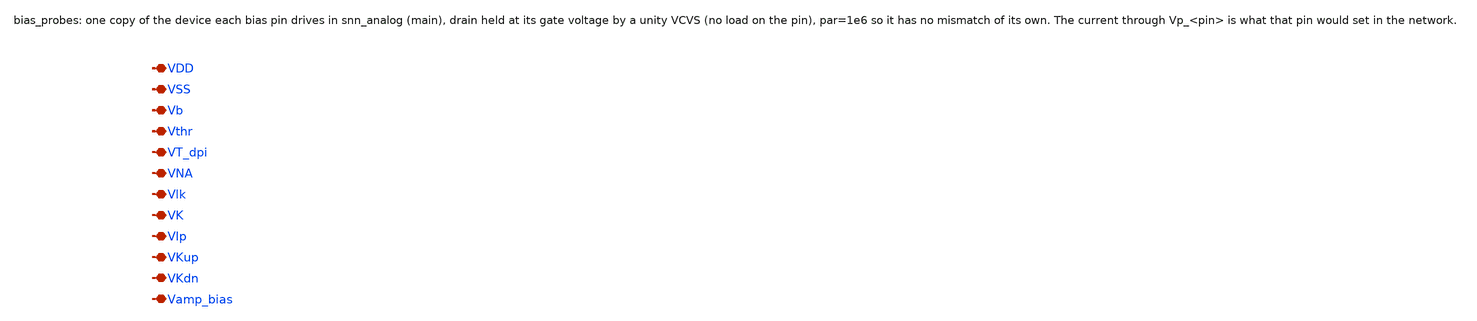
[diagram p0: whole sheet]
** sch_path: analog/bias/testbenches/bias_probes.sch
**.subckt bias_probes VDD VSS Vb Vthr VT_dpi VNA Vlk VK VIp VKup VKdn Vamp_bias
*.iopin VDD
*.iopin VSS
*.iopin Vb
*.iopin Vthr
*.iopin VT_dpi
*.iopin VNA
*.iopin Vlk
*.iopin VK
*.iopin VIp
*.iopin VKup
*.iopin VKdn
*.iopin Vamp_bias
**** begin user architecture code


* probe per bias pin: E holds the drain at the gate voltage, Vp measures the current
E_Vb pd_Vb VSS Vb VSS 1
X_Vb pd_Vb Vb ps_Vb VSS nfet_03v3 L=8.0u W=1.0u nf=1 par=1e6
Vp_Vb ps_Vb VSS 0
E_Vthr pd_Vthr VSS Vthr VSS 1
X_Vthr pd_Vthr Vthr ps_Vthr VDD pfet_03v3 L=0.28u W=0.22u nf=1 par=1e6
Vp_Vthr VDD ps_Vthr 0
E_VT_dpi pd_VT_dpi VSS VT_dpi VSS 1
X_VT_dpi pd_VT_dpi VT_dpi ps_VT_dpi VDD pfet_03v3 L=0.28u W=0.22u nf=1 par=1e6
Vp_VT_dpi VDD ps_VT_dpi 0
E_VNA pd_VNA VSS VNA VSS 1
X_VNA pd_VNA VNA ps_VNA VDD pfet_03v3 L=1.0u W=1.0u nf=1 par=1e6
Vp_VNA VDD ps_VNA 0
E_Vlk pd_Vlk VSS Vlk VSS 1
X_Vlk pd_Vlk Vlk ps_Vlk VSS nfet_03v3 L=1.0u W=1.0u nf=1 par=1e6
Vp_Vlk ps_Vlk VSS 0
E_VK pd_VK VSS VK VSS 1
X_VK pd_VK VK ps_VK VSS nfet_03v3 L=1.0u W=1.0u nf=1 par=1e6
Vp_VK ps_VK VSS 0
E_VIp pd_VIp VSS VIp VSS 1
X_VIp pd_VIp VIp ps_VIp VSS nfet_03v3 L=1.0u W=1.0u nf=1 par=1e6
Vp_VIp ps_VIp VSS 0
E_VKup pd_VKup VSS VKup VSS 1
X_VKup pd_VKup VKup ps_VKup VDD pfet_03v3 L=1.0u W=1.0u nf=1 par=1e6
Vp_VKup VDD ps_VKup 0
E_VKdn pd_VKdn VSS VKdn VSS 1
X_VKdn pd_VKdn VKdn ps_VKdn VSS nfet_03v3 L=1.0u W=1.0u nf=1 par=1e6
Vp_VKdn ps_VKdn VSS 0
E_Vamp_bias pd_Vamp_bias VSS Vamp_bias VSS 1
X_Vamp_bias pd_Vamp_bias Vamp_bias ps_Vamp_bias VSS nfet_03v3 L=0.28u W=0.22u nf=1 par=1e6
Vp_Vamp_bias ps_Vamp_bias VSS 0


**** end user architecture code
**.ends
.end
